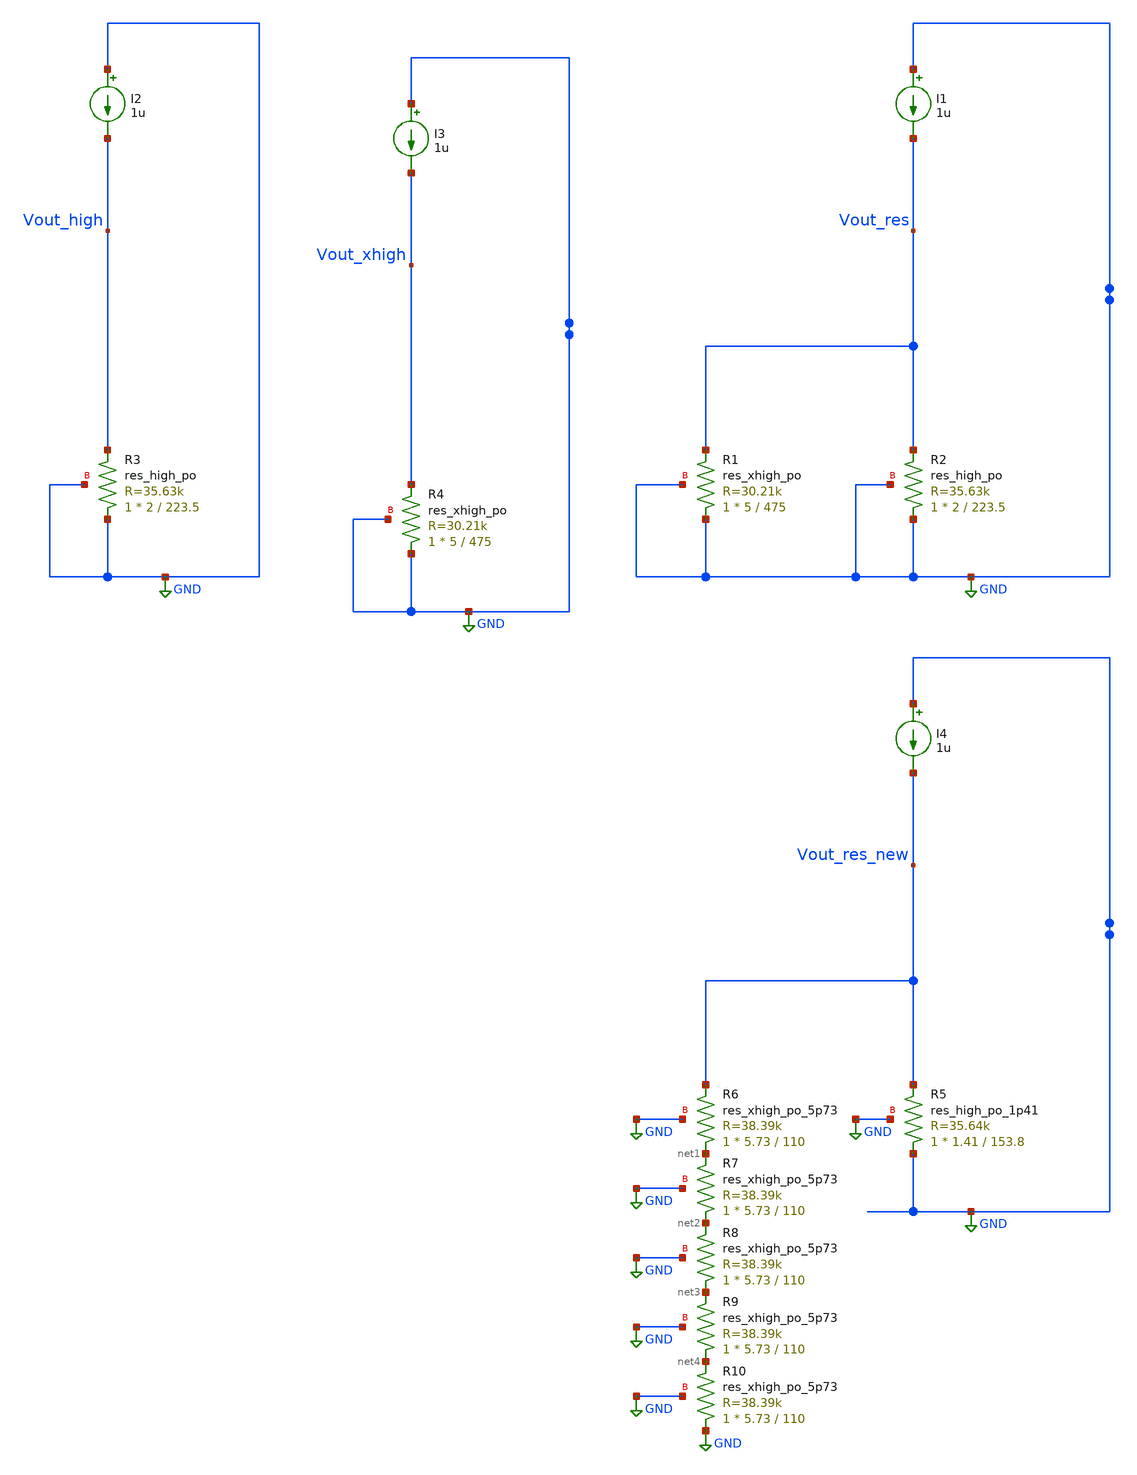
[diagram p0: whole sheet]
** sch_path: design/misc/testing/res_current_ref_para.sch
**.subckt res_current_ref_para
I1 GND Vout_res 1u
XR2 GND Vout_res GND sky130_fd_pr__res_high_po W=2 L=223.5 mult=1 m=1
XR1 GND Vout_res GND sky130_fd_pr__res_xhigh_po W=5 L=475 mult=1 m=1
I2 GND Vout_high 1u
XR3 GND Vout_high GND sky130_fd_pr__res_high_po W=2 L=223.5 mult=1 m=1
I3 GND Vout_xhigh 1u
XR4 GND Vout_xhigh GND sky130_fd_pr__res_xhigh_po W=5 L=475 mult=1 m=1
I4 GND Vout_res_new 1u
XR6 net1 Vout_res_new GND sky130_fd_pr__res_xhigh_po_5p73 L=110 mult=1 m=1
XR7 net2 net1 GND sky130_fd_pr__res_xhigh_po_5p73 L=110 mult=1 m=1
XR8 net3 net2 GND sky130_fd_pr__res_xhigh_po_5p73 L=110 mult=1 m=1
XR9 net4 net3 GND sky130_fd_pr__res_xhigh_po_5p73 L=110 mult=1 m=1
XR10 GND net4 GND sky130_fd_pr__res_xhigh_po_5p73 L=110 mult=1 m=1
XR5 GND Vout_res_new GND sky130_fd_pr__res_high_po_1p41 L=153.8 mult=1 m=1
**** begin user architecture code
.lib $::SKYWATER_MODELS/sky130.lib.spice tt


.param temp=27

.dc temp -20 100 1


.save all
.control
run
plot Vout_res Vout_res_new
plot deriv(Vout_res) deriv(Vout_res_new)
plot Vout_high
plot deriv(Vout_high)
plot Vout_xhigh
plot deriv(Vout_xhigh)
let Rcomb = Vout_high*Vout_xhigh/(Vout_high + Vout_xhigh)
plot Rcomb
let Isim = 1.2/Rcomb
plot Isim
let Rnom = Vout_high*Vout_xhigh
let Rdim = Vout_high + Vout_xhigh
plot Rnom
plot Rdim

.endc



**** end user architecture code
**.ends
.GLOBAL GND
.end
